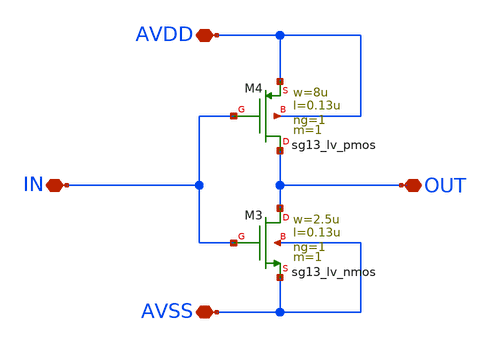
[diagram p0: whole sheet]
** sch_path: current_generator/analog/DAC/schematics/buffer.sch
**.subckt buffer AVDD AVSS IN OUT
*.iopin AVDD
*.iopin AVSS
*.iopin IN
*.iopin OUT
XM3 OUT IN AVSS AVSS sg13_lv_nmos w=2.5u l=0.13u ng=1 m=1 mm_ok=1
XM4 OUT IN AVDD AVDD sg13_lv_pmos w=8u l=0.13u ng=1 m=1 mm_ok=1
**.ends
.end
